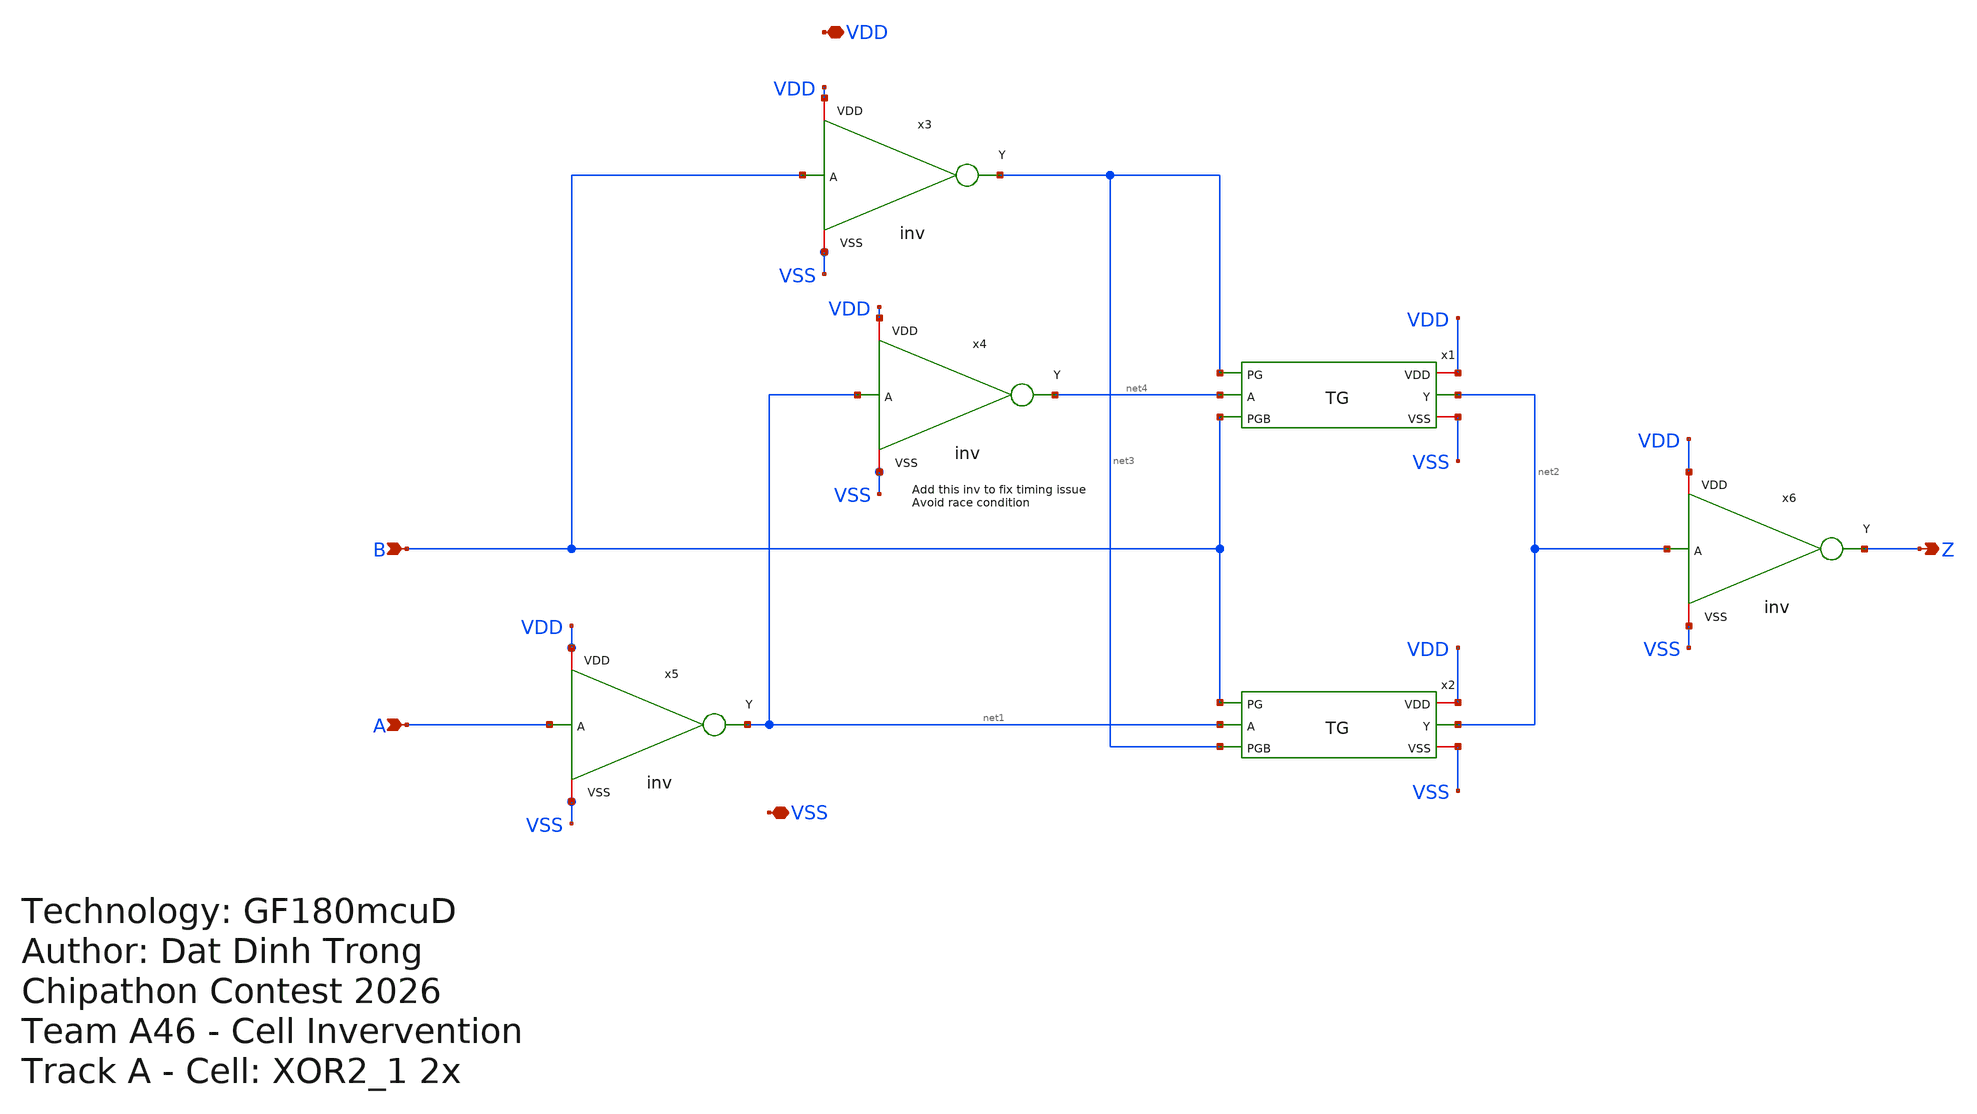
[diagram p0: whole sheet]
** sch_path: xschem/XOR2_1.sch
**.subckt XOR2_1 A B Z VDD VSS
*.ipin A
*.ipin B
*.opin Z
*.iopin VDD
*.iopin VSS
x1 net3 VDD net2 net4 VSS B TG
x2 B VDD net2 net1 VSS net3 TG
x3 VDD B net3 VSS inv
x4 VDD net1 net4 VSS inv
x5 VDD A net1 VSS inv
x6 VDD net2 Z VSS inv
**.ends
.end
